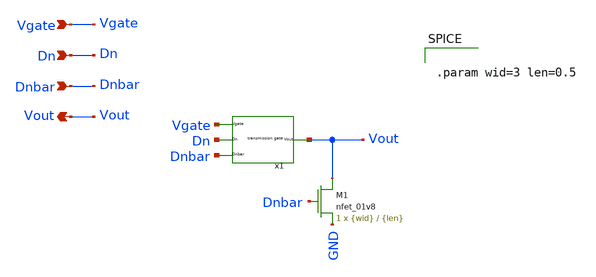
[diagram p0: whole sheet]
** sch_path: final/LDS/gate_driver_LDS.sch
**.subckt gate_driver_LDS Vgate Dn Vout Dnbar
*.ipin Vgate
*.ipin Dn
*.opin Vout
*.ipin Dnbar
XM1 Vout Dnbar GND GND sky130_fd_pr__nfet_01v8 L={len} W={wid} nf=1 ad='int((nf+1)/2) * W/nf * 0.29'
+ as='int((nf+2)/2) * W/nf * 0.29' pd='2*int((nf+1)/2) * (W/nf + 0.29)' ps='2*int((nf+2)/2) * (W/nf + 0.29)'
+ nrd='0.29 / W' nrs='0.29 / W' sa=0 sb=0 sd=0 mult=1 m=1
x1 Vgate Dn Dnbar Vout transmission_gate_LDS
**** begin user architecture code


.param wid=3 len=0.5


**** end user architecture code
**.ends

* expanding   symbol:  transmission_gate_LDS.sym # of pins=4
** sym_path: final/LDS/transmission_gate_LDS.sym
** sch_path: final/LDS/transmission_gate_LDS.sch
.subckt transmission_gate_LDS Vgate Dn Dnbar Vout
*.ipin Vgate
*.ipin Dn
*.ipin Dnbar
*.opin Vout
XM1 Vout Dn Vgate GND sky130_fd_pr__nfet_01v8 L={len} W={wid} nf=1 ad='int((nf+1)/2) * W/nf * 0.29' as='int((nf+2)/2) * W/nf * 0.29'
+ pd='2*int((nf+1)/2) * (W/nf + 0.29)' ps='2*int((nf+2)/2) * (W/nf + 0.29)' nrd='0.29 / W' nrs='0.29 / W'
+ sa=0 sb=0 sd=0 mult=1 m=1
XM2 Vout Dnbar Vgate VDD sky130_fd_pr__pfet_01v8 L={len} W={wid} nf=1 ad='int((nf+1)/2) * W/nf * 0.29'
+ as='int((nf+2)/2) * W/nf * 0.29' pd='2*int((nf+1)/2) * (W/nf + 0.29)' ps='2*int((nf+2)/2) * (W/nf + 0.29)'
+ nrd='0.29 / W' nrs='0.29 / W' sa=0 sb=0 sd=0 mult=1 m=1
**** begin user architecture code


.param wid=3 len=0.5


**** end user architecture code
.ends

.end
